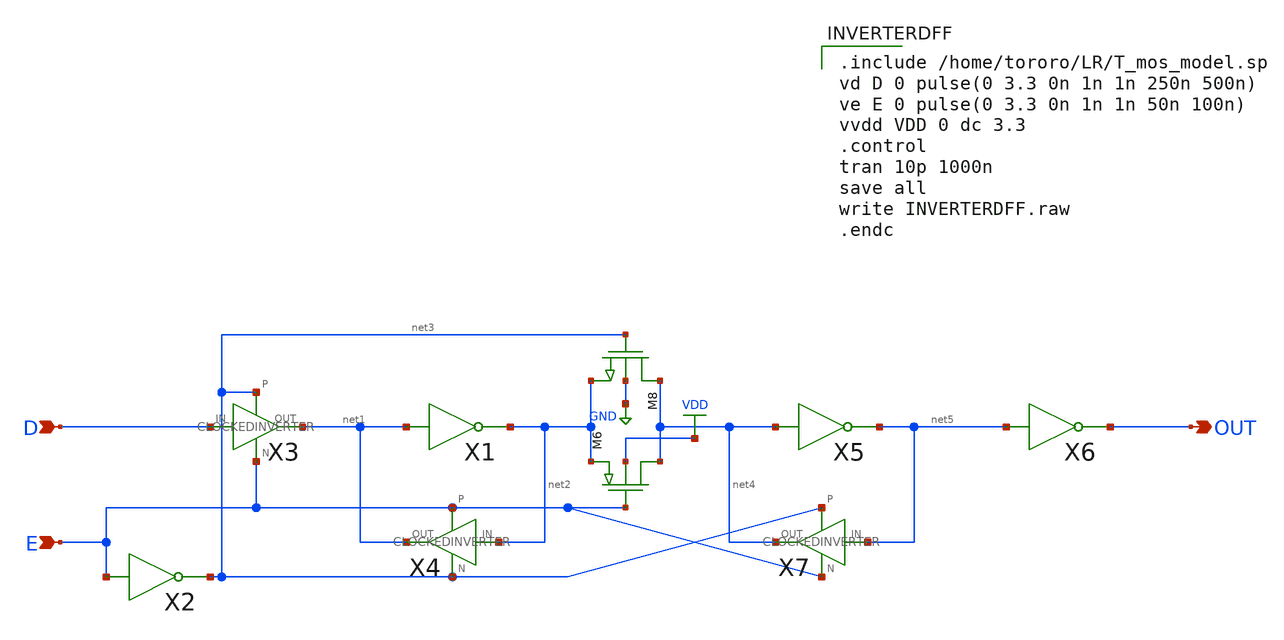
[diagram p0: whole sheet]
** sch_path: task_LATCH/INVERTERDFF.sch
**.subckt INVERTERDFF D OUT E
*.ipin D
*.opin OUT
*.ipin E
X1 net1 net2 INVERTER
X2 E net3 INVERTER
X3 D net1 net3 E CLOCKEDINVERTER
X4 net2 net1 E net3 CLOCKEDINVERTER
X5 net4 net5 INVERTER
X6 net5 OUT INVERTER
X7 net5 net4 net3 E CLOCKEDINVERTER
M6 net4 E net2 VDD pch w=10.5u l=0.35u as=0 ps=0 ad=0 pd=0 m=1
M8 net4 net3 net2 GND nch w=3.5u l=0.35u as=0 ps=0 ad=0 pd=0 m=1
**** begin user architecture code

.include /home/tororo/LR/T_mos_model.sp
vd D 0 pulse(0 3.3 0n 1n 1n 250n 500n)
ve E 0 pulse(0 3.3 0n 1n 1n 50n 100n)
vvdd VDD 0 dc 3.3
.control
tran 10p 1000n
save all
write INVERTERDFF.raw
.endc

**** end user architecture code
**.ends

* expanding   symbol:  LR/task_LATCH/INVERTER.sym # of pins=2
** sym_path: task_LATCH/INVERTER.sym
** sch_path: task_LATCH/INVERTER.sch
.subckt INVERTER IN OUT
*.opin OUT
*.ipin IN
M6 OUT IN VDD VDD pch w=10.5u l=0.35u as=0 ps=0 ad=0 pd=0 m=1
M8 OUT IN GND GND nch w=3.5u l=0.35u as=0 ps=0 ad=0 pd=0 m=1
.ends


* expanding   symbol:  LR/task_LATCH/CLOCKEDINVERTER.sym # of pins=4
** sym_path: task_LATCH/CLOCKEDINVERTER.sym
** sch_path: task_LATCH/CLOCKEDINVERTER.sch
.subckt CLOCKEDINVERTER IN OUT P N
*.opin OUT
*.ipin IN
*.ipin P
*.ipin N
M6 OUT IN net1 VDD pch w=10.5u l=0.35u as=0 ps=0 ad=0 pd=0 m=1
M8 OUT IN net2 GND nch w=3.5u l=0.35u as=0 ps=0 ad=0 pd=0 m=1
M1 net1 P VDD VDD pch w=10.5u l=0.35u as=0 ps=0 ad=0 pd=0 m=1
M2 net2 N GND GND nch w=3.5u l=0.35u as=0 ps=0 ad=0 pd=0 m=1
.ends

.GLOBAL VDD
.GLOBAL GND
.end
